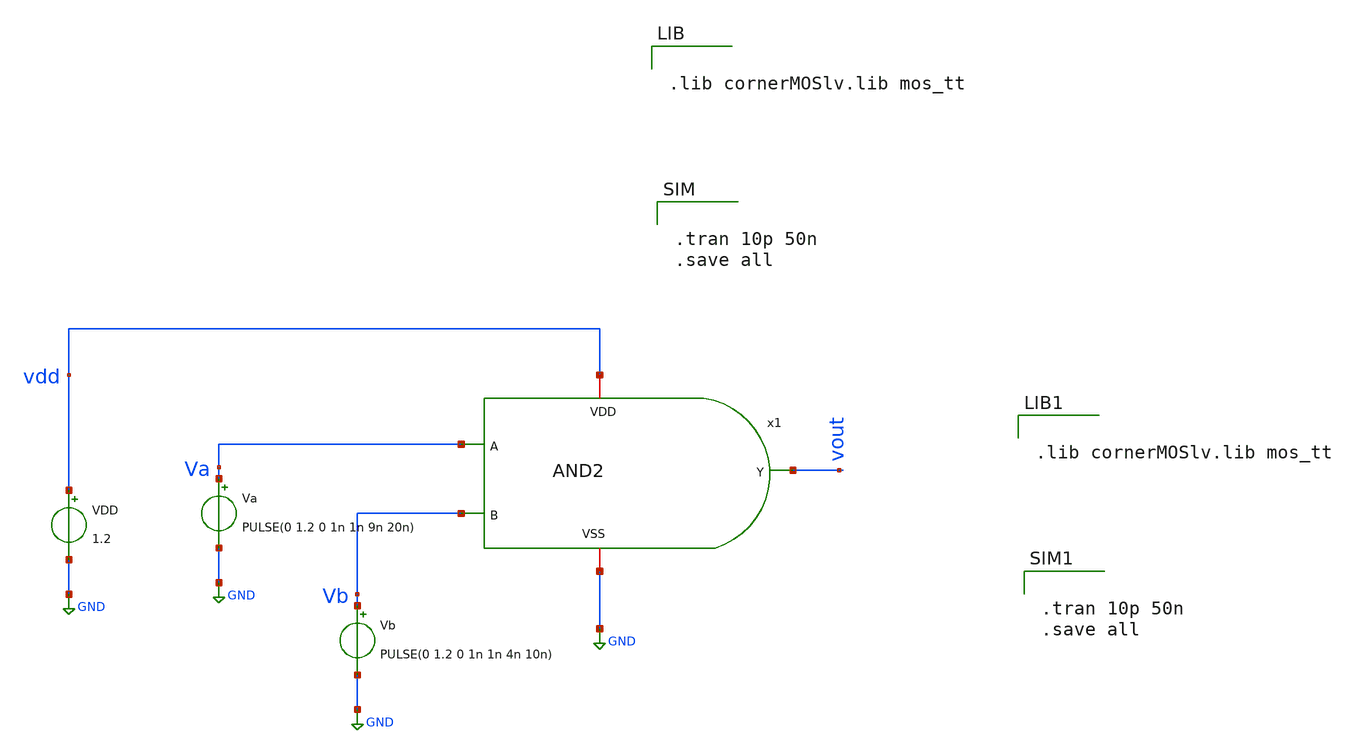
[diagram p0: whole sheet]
** sch_path: TestAND.sch
**.subckt TestAND
Va Va GND PULSE(0 1.2 0 1n 1n 9n 20n)
VDD vdd GND 1.2
Vb Vb GND PULSE(0 1.2 0 1n 1n 4n 10n)
x1 vdd Va vout Vb GND AND2
**** begin user architecture code


.lib cornerMOSlv.lib mos_tt




.tran 10p 50n
.save all




.lib cornerMOSlv.lib mos_tt




.tran 10p 50n
.save all


**** end user architecture code
**.ends
.GLOBAL GND
.end
